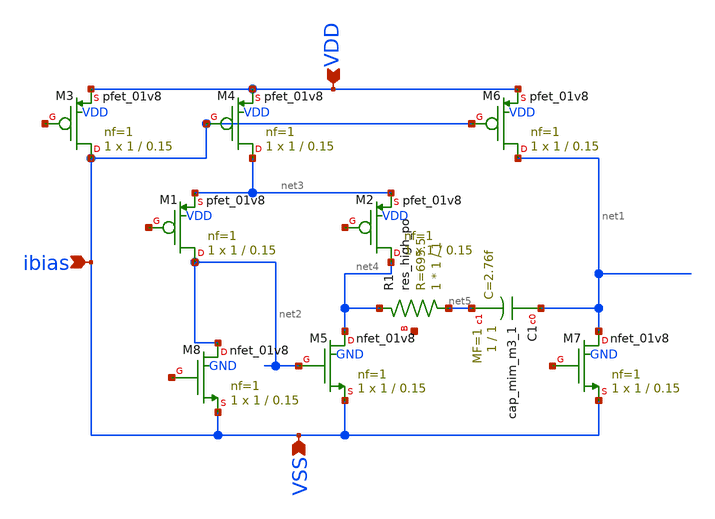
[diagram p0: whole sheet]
** sch_path: analog/bootcamp_opamp/schematics/opamp_two_stage.sch
**.subckt opamp_two_stage ibias VDD VSS
*.ipin ibias
*.ipin VDD
*.ipin VSS
XM3 ibias net6 VDD VDD sky130_fd_pr__pfet_01v8 L=0.15 W=1 nf=1 ad='int((nf+1)/2) * W/nf * 0.29' as='int((nf+2)/2) * W/nf * 0.29'
+ pd='2*int((nf+1)/2) * (W/nf + 0.29)' ps='2*int((nf+2)/2) * (W/nf + 0.29)' nrd='0.29 / W' nrs='0.29 / W'
+ sa=0 sb=0 sd=0 mult=1 m=1
XM4 net3 ibias VDD VDD sky130_fd_pr__pfet_01v8 L=0.15 W=1 nf=1 ad='int((nf+1)/2) * W/nf * 0.29' as='int((nf+2)/2) * W/nf * 0.29'
+ pd='2*int((nf+1)/2) * (W/nf + 0.29)' ps='2*int((nf+2)/2) * (W/nf + 0.29)' nrd='0.29 / W' nrs='0.29 / W'
+ sa=0 sb=0 sd=0 mult=1 m=1
XM5 net4 net2 ibias GND sky130_fd_pr__nfet_01v8 L=0.15 W=1 nf=1 ad='int((nf+1)/2) * W/nf * 0.29' as='int((nf+2)/2) * W/nf * 0.29'
+ pd='2*int((nf+1)/2) * (W/nf + 0.29)' ps='2*int((nf+2)/2) * (W/nf + 0.29)' nrd='0.29 / W' nrs='0.29 / W'
+ sa=0 sb=0 sd=0 mult=1 m=1
XM6 net1 ibias VDD VDD sky130_fd_pr__pfet_01v8 L=0.15 W=1 nf=1 ad='int((nf+1)/2) * W/nf * 0.29' as='int((nf+2)/2) * W/nf * 0.29'
+ pd='2*int((nf+1)/2) * (W/nf + 0.29)' ps='2*int((nf+2)/2) * (W/nf + 0.29)' nrd='0.29 / W' nrs='0.29 / W'
+ sa=0 sb=0 sd=0 mult=1 m=1
XM7 net1 net7 ibias GND sky130_fd_pr__nfet_01v8 L=0.15 W=1 nf=1 ad='int((nf+1)/2) * W/nf * 0.29' as='int((nf+2)/2) * W/nf * 0.29'
+ pd='2*int((nf+1)/2) * (W/nf + 0.29)' ps='2*int((nf+2)/2) * (W/nf + 0.29)' nrd='0.29 / W' nrs='0.29 / W'
+ sa=0 sb=0 sd=0 mult=1 m=1
XM8 net2 net8 ibias GND sky130_fd_pr__nfet_01v8 L=0.15 W=1 nf=1 ad='int((nf+1)/2) * W/nf * 0.29' as='int((nf+2)/2) * W/nf * 0.29'
+ pd='2*int((nf+1)/2) * (W/nf + 0.29)' ps='2*int((nf+2)/2) * (W/nf + 0.29)' nrd='0.29 / W' nrs='0.29 / W'
+ sa=0 sb=0 sd=0 mult=1 m=1
XR1 net5 net4 net9 sky130_fd_pr__res_high_po W=1 L=1 mult=1 m=1
XC1 net1 net5 sky130_fd_pr__cap_mim_m3_1 W=1 L=1 MF=1 m=1
XM1 net2 net10 net3 VDD sky130_fd_pr__pfet_01v8 L=0.15 W=1 nf=1 ad='int((nf+1)/2) * W/nf * 0.29' as='int((nf+2)/2) * W/nf * 0.29'
+ pd='2*int((nf+1)/2) * (W/nf + 0.29)' ps='2*int((nf+2)/2) * (W/nf + 0.29)' nrd='0.29 / W' nrs='0.29 / W'
+ sa=0 sb=0 sd=0 mult=1 m=1
XM2 net4 net11 net3 VDD sky130_fd_pr__pfet_01v8 L=0.15 W=1 nf=1 ad='int((nf+1)/2) * W/nf * 0.29' as='int((nf+2)/2) * W/nf * 0.29'
+ pd='2*int((nf+1)/2) * (W/nf + 0.29)' ps='2*int((nf+2)/2) * (W/nf + 0.29)' nrd='0.29 / W' nrs='0.29 / W'
+ sa=0 sb=0 sd=0 mult=1 m=1
**.ends
.end
